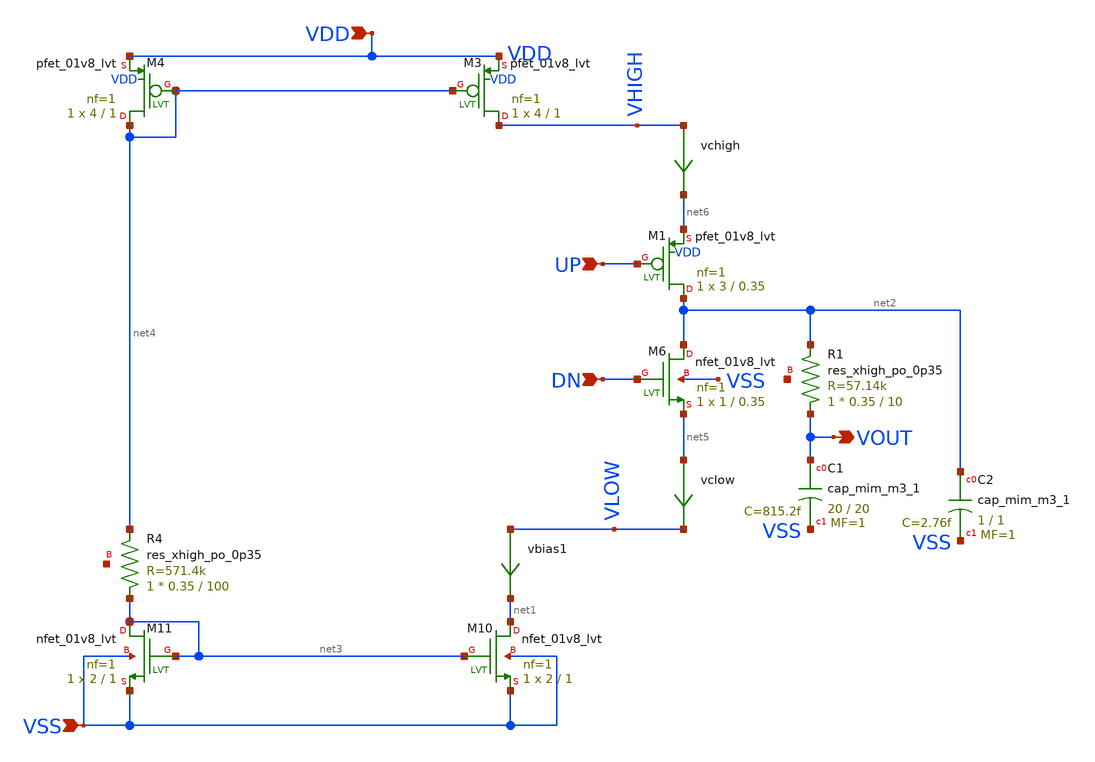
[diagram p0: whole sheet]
** sch_path: xschem/pll_cp_beta.sch
**.subckt pll_cp_beta UP DN VOUT VDD VSS
*.ipin UP
*.ipin DN
*.opin VOUT
*.ipin VDD
*.ipin VSS
XM6 net2 DN net5 VSS sky130_fd_pr__nfet_01v8_lvt L=0.35 W=1 nf=1 ad='int((nf+1)/2) * W/nf * 0.29' as='int((nf+2)/2) * W/nf * 0.29'
+ pd='2*int((nf+1)/2) * (W/nf + 0.29)' ps='2*int((nf+2)/2) * (W/nf + 0.29)' nrd='0.29 / W' nrs='0.29 / W'
+ sa=0 sb=0 sd=0 mult=1 m=1
XM10 net1 net3 VSS VSS sky130_fd_pr__nfet_01v8_lvt L=1 W=2 nf=1 ad='int((nf+1)/2) * W/nf * 0.29' as='int((nf+2)/2) * W/nf * 0.29'
+ pd='2*int((nf+1)/2) * (W/nf + 0.29)' ps='2*int((nf+2)/2) * (W/nf + 0.29)' nrd='0.29 / W' nrs='0.29 / W'
+ sa=0 sb=0 sd=0 mult=1 m=1
vbias1 VLOW net1 0
.save i(vbias1)
XM1 net2 UP net6 VDD sky130_fd_pr__pfet_01v8_lvt L=0.35 W=3 nf=1 ad='int((nf+1)/2) * W/nf * 0.29' as='int((nf+2)/2) * W/nf * 0.29'
+ pd='2*int((nf+1)/2) * (W/nf + 0.29)' ps='2*int((nf+2)/2) * (W/nf + 0.29)' nrd='0.29 / W' nrs='0.29 / W'
+ sa=0 sb=0 sd=0 mult=1 m=1
XC1 VOUT VSS sky130_fd_pr__cap_mim_m3_1 W=20 L=20 MF=1 m=1
XM11 net3 net3 VSS VSS sky130_fd_pr__nfet_01v8_lvt L=1 W=2 nf=1 ad='int((nf+1)/2) * W/nf * 0.29' as='int((nf+2)/2) * W/nf * 0.29'
+ pd='2*int((nf+1)/2) * (W/nf + 0.29)' ps='2*int((nf+2)/2) * (W/nf + 0.29)' nrd='0.29 / W' nrs='0.29 / W'
+ sa=0 sb=0 sd=0 mult=1 m=1
XR4 net3 net4 net7 sky130_fd_pr__res_xhigh_po_0p35 L=100 mult=1 m=1
XM3 VHIGH net4 VDD VDD sky130_fd_pr__pfet_01v8_lvt L=1 W=4 nf=1 ad='int((nf+1)/2) * W/nf * 0.29' as='int((nf+2)/2) * W/nf * 0.29'
+ pd='2*int((nf+1)/2) * (W/nf + 0.29)' ps='2*int((nf+2)/2) * (W/nf + 0.29)' nrd='0.29 / W' nrs='0.29 / W'
+ sa=0 sb=0 sd=0 mult=1 m=1
XM4 net4 net4 VDD VDD sky130_fd_pr__pfet_01v8_lvt L=1 W=4 nf=1 ad='int((nf+1)/2) * W/nf * 0.29' as='int((nf+2)/2) * W/nf * 0.29'
+ pd='2*int((nf+1)/2) * (W/nf + 0.29)' ps='2*int((nf+2)/2) * (W/nf + 0.29)' nrd='0.29 / W' nrs='0.29 / W'
+ sa=0 sb=0 sd=0 mult=1 m=1
vclow net5 VLOW 0
.save i(vclow)
vchigh VHIGH net6 0
.save i(vchigh)
XC2 net2 VSS sky130_fd_pr__cap_mim_m3_1 W=1 L=1 MF=1 m=1
XR1 VOUT net2 net8 sky130_fd_pr__res_xhigh_po_0p35 L=10 mult=1 m=1
**.ends
.end
